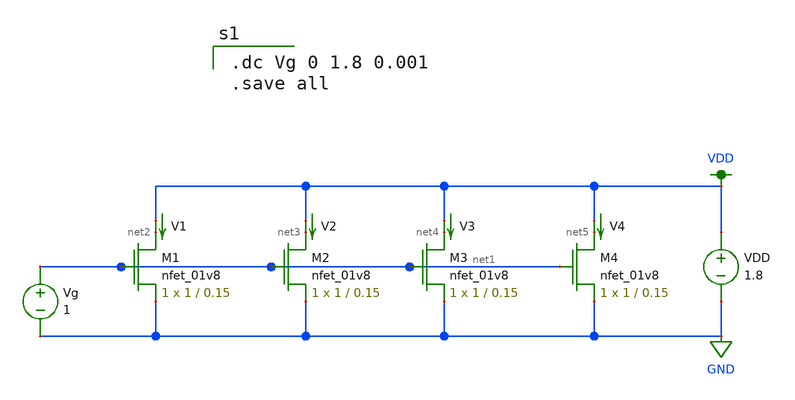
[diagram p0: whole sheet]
** sch_path: mp4/xschem/monte_carlo_test/nmos_4x.sch
**.subckt nmos_4x
V1 VDD net2 0
.save i(v1)
V2 VDD net3 0
.save i(v2)
V3 VDD net4 0
.save i(v3)
V4 VDD net5 0
.save i(v4)
Vg net1 GND 1
VDD VDD GND 1.8
XM1 net2 net1 GND GND sky130_fd_pr__nfet_01v8 L=0.15 W=1 nf=1 ad='int((nf+1)/2) * W/nf * 0.29' as='int((nf+2)/2) * W/nf * 0.29'
+ pd='2*int((nf+1)/2) * (W/nf + 0.29)' ps='2*int((nf+2)/2) * (W/nf + 0.29)' nrd='0.29 / W' nrs='0.29 / W'
+ sa=0 sb=0 sd=0 mult=1 m=1
XM2 net3 net1 GND GND sky130_fd_pr__nfet_01v8 L=0.15 W=1 nf=1 ad='int((nf+1)/2) * W/nf * 0.29' as='int((nf+2)/2) * W/nf * 0.29'
+ pd='2*int((nf+1)/2) * (W/nf + 0.29)' ps='2*int((nf+2)/2) * (W/nf + 0.29)' nrd='0.29 / W' nrs='0.29 / W'
+ sa=0 sb=0 sd=0 mult=1 m=1
XM3 net4 net1 GND GND sky130_fd_pr__nfet_01v8 L=0.15 W=1 nf=1 ad='int((nf+1)/2) * W/nf * 0.29' as='int((nf+2)/2) * W/nf * 0.29'
+ pd='2*int((nf+1)/2) * (W/nf + 0.29)' ps='2*int((nf+2)/2) * (W/nf + 0.29)' nrd='0.29 / W' nrs='0.29 / W'
+ sa=0 sb=0 sd=0 mult=1 m=1
XM4 net5 net1 GND GND sky130_fd_pr__nfet_01v8 L=0.15 W=1 nf=1 ad='int((nf+1)/2) * W/nf * 0.29' as='int((nf+2)/2) * W/nf * 0.29'
+ pd='2*int((nf+1)/2) * (W/nf + 0.29)' ps='2*int((nf+2)/2) * (W/nf + 0.29)' nrd='0.29 / W' nrs='0.29 / W'
+ sa=0 sb=0 sd=0 mult=1 m=1
**** begin user architecture code

.option wnflag=1
.param MC_SWITCH=1.0
.lib ~/skywater/skywater-pdk/libraries/sky130_fd_pr_ngspice/latest/models/sky130.lib.spice tt


.dc Vg 0 1.8 0.001
.save all

**** end user architecture code
**.ends
.GLOBAL GND
.GLOBAL VDD
.end
